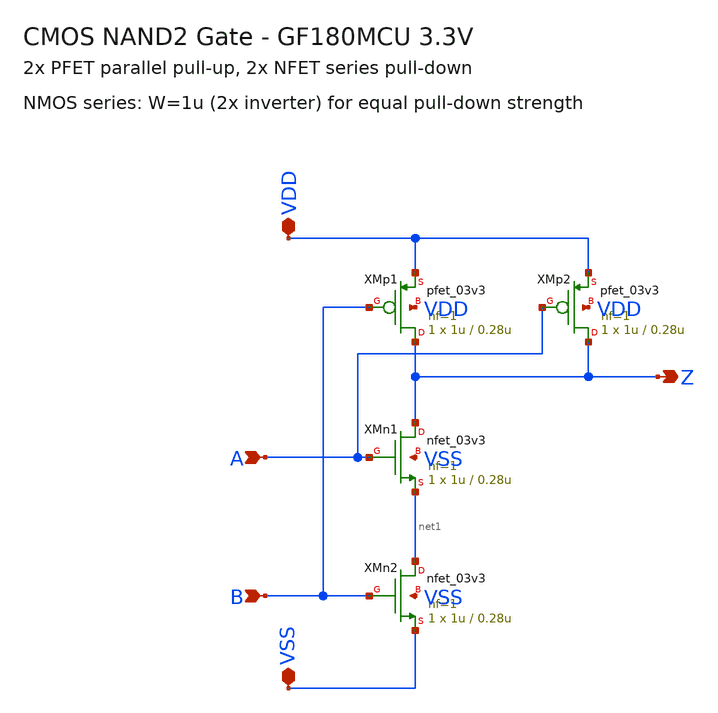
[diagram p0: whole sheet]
** sch_path: designs/libs/PDF/nand_pf.sch
**.subckt nand_pf VDD A Z B VSS
*.iopin VDD
*.ipin A
*.opin Z
*.ipin B
*.iopin VSS
XMp1 Z B VDD VDD pfet_03v3 L=0.28u W=1u nf=1 ad='int((nf+1)/2) * W/nf * 0.18u' as='int((nf+2)/2) * W/nf * 0.18u'
+ pd='2*int((nf+1)/2) * (W/nf + 0.18u)' ps='2*int((nf+2)/2) * (W/nf + 0.18u)' nrd='0.18u / W' nrs='0.18u / W'
+ sa=0 sb=0 sd=0 m=1
XMp2 Z A VDD VDD pfet_03v3 L=0.28u W=1u nf=1 ad='int((nf+1)/2) * W/nf * 0.18u' as='int((nf+2)/2) * W/nf * 0.18u'
+ pd='2*int((nf+1)/2) * (W/nf + 0.18u)' ps='2*int((nf+2)/2) * (W/nf + 0.18u)' nrd='0.18u / W' nrs='0.18u / W'
+ sa=0 sb=0 sd=0 m=1
XMn1 Z A net1 VSS nfet_03v3 L=0.28u W=1u nf=1 ad='int((nf+1)/2) * W/nf * 0.18u' as='int((nf+2)/2) * W/nf * 0.18u'
+ pd='2*int((nf+1)/2) * (W/nf + 0.18u)' ps='2*int((nf+2)/2) * (W/nf + 0.18u)' nrd='0.18u / W' nrs='0.18u / W'
+ sa=0 sb=0 sd=0 m=1
XMn2 net1 B VSS VSS nfet_03v3 L=0.28u W=1u nf=1 ad='int((nf+1)/2) * W/nf * 0.18u' as='int((nf+2)/2) * W/nf * 0.18u'
+ pd='2*int((nf+1)/2) * (W/nf + 0.18u)' ps='2*int((nf+2)/2) * (W/nf + 0.18u)' nrd='0.18u / W' nrs='0.18u / W'
+ sa=0 sb=0 sd=0 m=1
**.ends
.end
